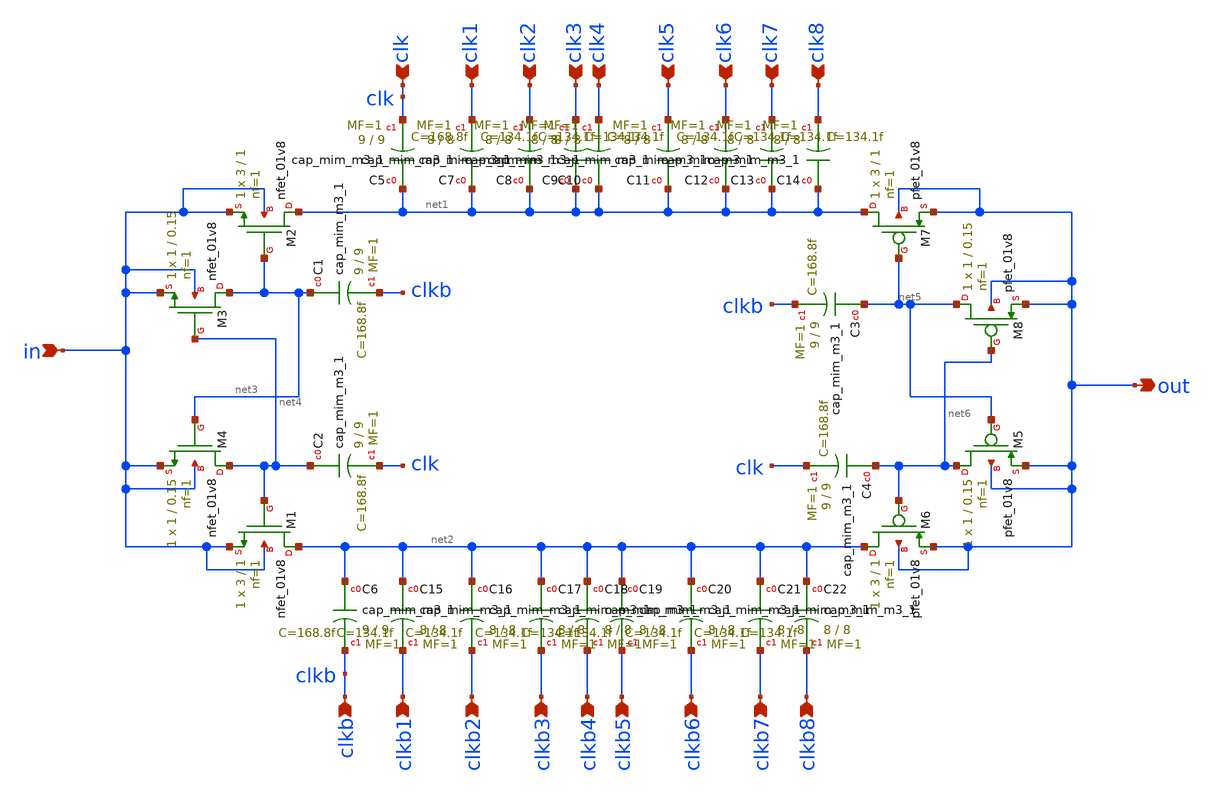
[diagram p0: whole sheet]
** sch_path: xschem/CP1.sch
**.subckt CP1 in clk clk1 clk2 clk3 clk4 clk5 clk6 clk7 clk8 clkb clkb1 clkb2 clkb3 clkb4 clkb5
*+ clkb6 clkb7 clkb8 out
*.ipin in
*.ipin clk
*.ipin clk1
*.ipin clk2
*.ipin clk3
*.ipin clk4
*.ipin clk5
*.ipin clk6
*.ipin clk7
*.ipin clk8
*.ipin clkb
*.ipin clkb1
*.ipin clkb2
*.ipin clkb3
*.ipin clkb4
*.ipin clkb5
*.ipin clkb6
*.ipin clkb7
*.ipin clkb8
*.opin out
XM2 net1 net3 in in sky130_fd_pr__nfet_01v8 L=1 W=3 nf=1 ad='int((nf+1)/2) * W/nf * 0.29' as='int((nf+2)/2) * W/nf * 0.29'
+ pd='2*int((nf+1)/2) * (W/nf + 0.29)' ps='2*int((nf+2)/2) * (W/nf + 0.29)' nrd='0.29 / W' nrs='0.29 / W'
+ sa=0 sb=0 sd=0 mult=1 m=1
XM1 net2 net4 in in sky130_fd_pr__nfet_01v8 L=1 W=3 nf=1 ad='int((nf+1)/2) * W/nf * 0.29' as='int((nf+2)/2) * W/nf * 0.29'
+ pd='2*int((nf+1)/2) * (W/nf + 0.29)' ps='2*int((nf+2)/2) * (W/nf + 0.29)' nrd='0.29 / W' nrs='0.29 / W'
+ sa=0 sb=0 sd=0 mult=1 m=1
XM3 net3 net4 in in sky130_fd_pr__nfet_01v8 L=0.15 W=1 nf=1 ad='int((nf+1)/2) * W/nf * 0.29' as='int((nf+2)/2) * W/nf * 0.29'
+ pd='2*int((nf+1)/2) * (W/nf + 0.29)' ps='2*int((nf+2)/2) * (W/nf + 0.29)' nrd='0.29 / W' nrs='0.29 / W'
+ sa=0 sb=0 sd=0 mult=1 m=1
XM4 net4 net3 in in sky130_fd_pr__nfet_01v8 L=0.15 W=1 nf=1 ad='int((nf+1)/2) * W/nf * 0.29' as='int((nf+2)/2) * W/nf * 0.29'
+ pd='2*int((nf+1)/2) * (W/nf + 0.29)' ps='2*int((nf+2)/2) * (W/nf + 0.29)' nrd='0.29 / W' nrs='0.29 / W'
+ sa=0 sb=0 sd=0 mult=1 m=1
XM5 net6 net5 out out sky130_fd_pr__pfet_01v8 L=0.15 W=1 nf=1 ad='int((nf+1)/2) * W/nf * 0.29' as='int((nf+2)/2) * W/nf * 0.29'
+ pd='2*int((nf+1)/2) * (W/nf + 0.29)' ps='2*int((nf+2)/2) * (W/nf + 0.29)' nrd='0.29 / W' nrs='0.29 / W'
+ sa=0 sb=0 sd=0 mult=1 m=1
XM6 net2 net6 out out sky130_fd_pr__pfet_01v8 L=1 W=3 nf=1 ad='int((nf+1)/2) * W/nf * 0.29' as='int((nf+2)/2) * W/nf * 0.29'
+ pd='2*int((nf+1)/2) * (W/nf + 0.29)' ps='2*int((nf+2)/2) * (W/nf + 0.29)' nrd='0.29 / W' nrs='0.29 / W'
+ sa=0 sb=0 sd=0 mult=1 m=1
XM7 net1 net5 out out sky130_fd_pr__pfet_01v8 L=1 W=3 nf=1 ad='int((nf+1)/2) * W/nf * 0.29' as='int((nf+2)/2) * W/nf * 0.29'
+ pd='2*int((nf+1)/2) * (W/nf + 0.29)' ps='2*int((nf+2)/2) * (W/nf + 0.29)' nrd='0.29 / W' nrs='0.29 / W'
+ sa=0 sb=0 sd=0 mult=1 m=1
XM8 net5 net6 out out sky130_fd_pr__pfet_01v8 L=0.15 W=1 nf=1 ad='int((nf+1)/2) * W/nf * 0.29' as='int((nf+2)/2) * W/nf * 0.29'
+ pd='2*int((nf+1)/2) * (W/nf + 0.29)' ps='2*int((nf+2)/2) * (W/nf + 0.29)' nrd='0.29 / W' nrs='0.29 / W'
+ sa=0 sb=0 sd=0 mult=1 m=1
XC1 net3 clkb sky130_fd_pr__cap_mim_m3_1 W=9 L=9 MF=1 m=1
XC2 net4 clk sky130_fd_pr__cap_mim_m3_1 W=9 L=9 MF=1 m=1
XC3 net5 clkb sky130_fd_pr__cap_mim_m3_1 W=9 L=9 MF=1 m=1
XC4 net6 clk sky130_fd_pr__cap_mim_m3_1 W=9 L=9 MF=1 m=1
XC5 net1 clk sky130_fd_pr__cap_mim_m3_1 W=9 L=9 MF=1 m=1
XC6 net2 clkb sky130_fd_pr__cap_mim_m3_1 W=9 L=9 MF=1 m=1
XC7 net1 clk1 sky130_fd_pr__cap_mim_m3_1 W=8 L=8 MF=1 m=1
XC8 net1 clk2 sky130_fd_pr__cap_mim_m3_1 W=8 L=8 MF=1 m=1
XC9 net1 clk3 sky130_fd_pr__cap_mim_m3_1 W=8 L=8 MF=1 m=1
XC10 net1 clk4 sky130_fd_pr__cap_mim_m3_1 W=8 L=8 MF=1 m=1
XC11 net1 clk5 sky130_fd_pr__cap_mim_m3_1 W=8 L=8 MF=1 m=1
XC12 net1 clk6 sky130_fd_pr__cap_mim_m3_1 W=8 L=8 MF=1 m=1
XC13 net1 clk7 sky130_fd_pr__cap_mim_m3_1 W=8 L=8 MF=1 m=1
XC14 net1 clk8 sky130_fd_pr__cap_mim_m3_1 W=8 L=8 MF=1 m=1
XC15 net2 clkb1 sky130_fd_pr__cap_mim_m3_1 W=8 L=8 MF=1 m=1
XC16 net2 clkb2 sky130_fd_pr__cap_mim_m3_1 W=8 L=8 MF=1 m=1
XC17 net2 clkb3 sky130_fd_pr__cap_mim_m3_1 W=8 L=8 MF=1 m=1
XC18 net2 clkb4 sky130_fd_pr__cap_mim_m3_1 W=8 L=8 MF=1 m=1
XC19 net2 clkb5 sky130_fd_pr__cap_mim_m3_1 W=8 L=8 MF=1 m=1
XC20 net2 clkb6 sky130_fd_pr__cap_mim_m3_1 W=8 L=8 MF=1 m=1
XC21 net2 clkb7 sky130_fd_pr__cap_mim_m3_1 W=8 L=8 MF=1 m=1
XC22 net2 clkb8 sky130_fd_pr__cap_mim_m3_1 W=8 L=8 MF=1 m=1
**.ends
.end
